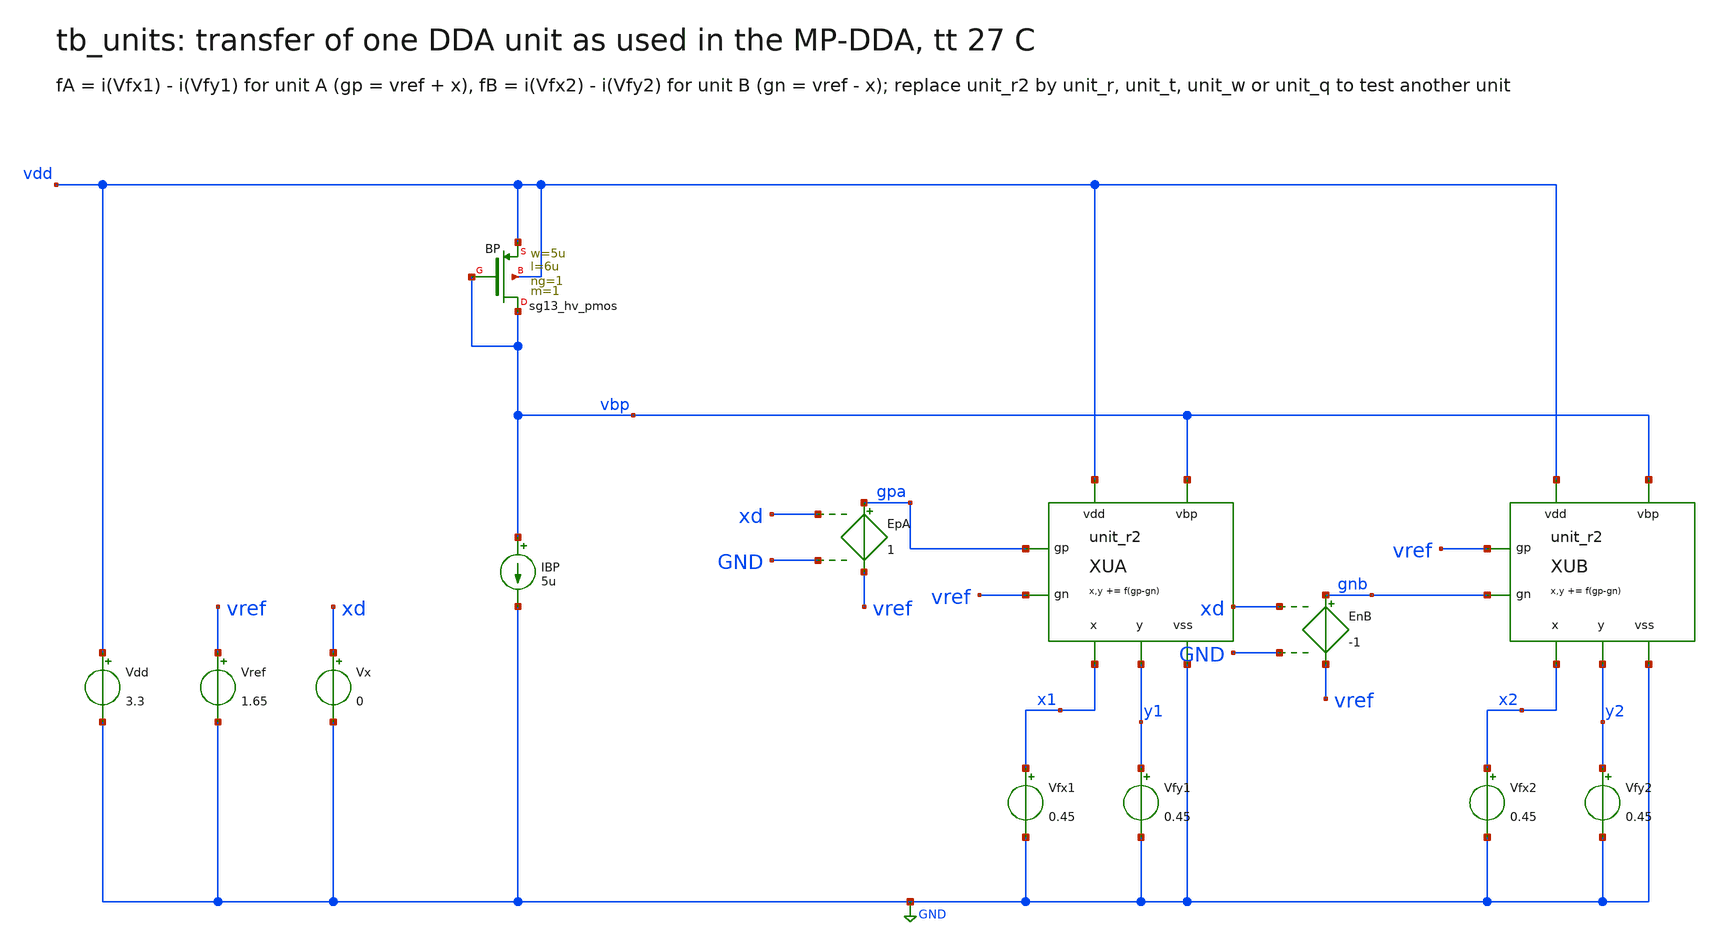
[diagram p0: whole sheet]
** sch_path: sudelbuecher/design_considerations/class_ab_pad_driver/improvements/xschem/tb_units.sch
**.subckt tb_units
Vdd vdd GND 3.3
Vref vref GND 1.65
Vx xd GND 0
XBP vbp vbp vdd vdd sg13_hv_pmos w=5u l=6u ng=1 m=1 mm_ok=1
IBP vbp GND 5u
XUA x1 y1 gpa vref vdd GND vbp unit_r2
Vfx1 x1 GND 0.45
Vfy1 y1 GND 0.45
EpA gpa vref xd GND 1
XUB x2 y2 vref gnb vdd GND vbp unit_r2
Vfx2 x2 GND 0.45
Vfy2 y2 GND 0.45
EnB gnb vref xd GND -1
**** begin user architecture code

.lib cornerMOShv.lib mos_tt
.lib cornerRES.lib res_typ
.param wwi=4u lwi=4u
.control
dc Vx -0.8 0.8 0.005
let fA = i(Vfx1) - i(Vfy1)
let fB = i(Vfx2) - i(Vfy2)
meas dc fa05 find fA at=0.5
meas dc fb05 find fB at=0.5
meas dc fam05 find fA at=-0.5
meas dc fbm05 find fB at=-0.5
print fa05 fb05 fam05 fbm05
if $?batchmode = 0
  plot fA fB
  plot fA-fB
end
.endc

**** end user architecture code
**.ends

* expanding   symbol:  unit_r2.sym # of pins=7
** sym_path: sudelbuecher/design_considerations/class_ab_pad_driver/improvements/xschem/unit_r2.sym
** sch_path: sudelbuecher/design_considerations/class_ab_pad_driver/improvements/xschem/unit_r2.sch
.subckt unit_r2 x y gp gn vdd vss vbp
*.opin x
*.opin y
*.ipin gp
*.ipin gn
*.iopin vdd
*.iopin vss
*.ipin vbp
XTa sa vbp vdd vdd sg13_hv_pmos w=5u l=6u ng=1 m=1 mm_ok=1
XTb sb vbp vdd vdd sg13_hv_pmos w=5u l=6u ng=1 m=1 mm_ok=1
XMa y gp sa sa sg13_hv_pmos w=20u l=1u ng=2 m=1 mm_ok=1
XMb x gn sb sb sg13_hv_pmos w=20u l=1u ng=2 m=1 mm_ok=1
XR sa sb vss rhigh w=0.5u l=50.6u m=1 b=0 mm_ok=1
.ends

.GLOBAL GND
.end
